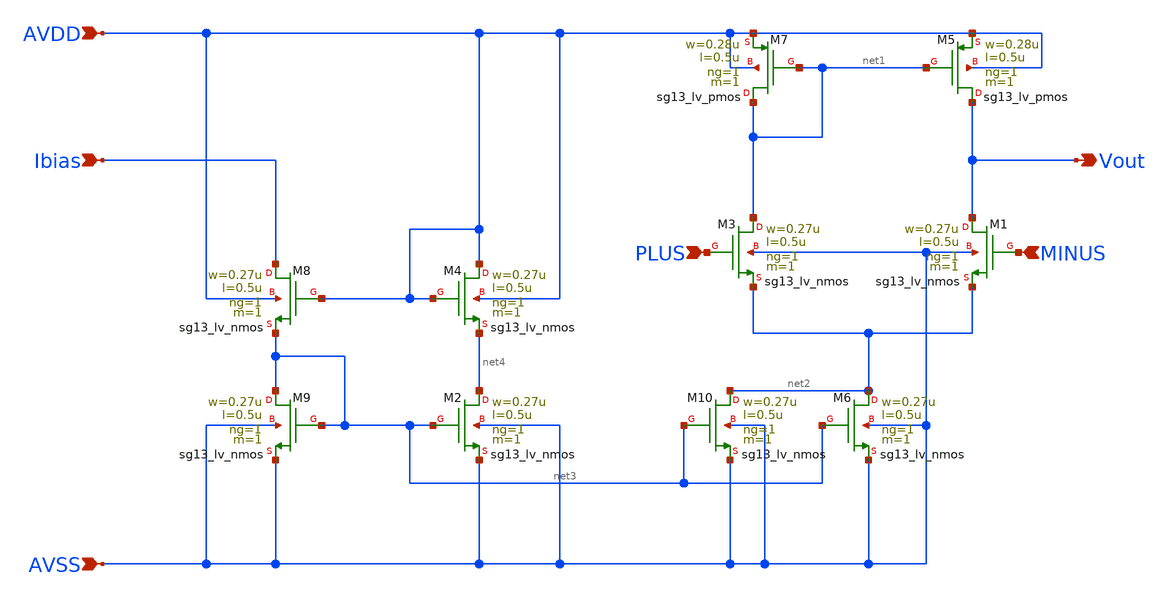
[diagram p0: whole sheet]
** sch_path: Designs/otas/5t_ota.sch
* (c) 2025 Thesis_HP, Apache-2.0 license
**.subckt 5t_ota PLUS MINUS Vout AVDD AVSS Ibias
*.ipin PLUS
*.ipin MINUS
*.opin Vout
*.ipin AVDD
*.ipin AVSS
*.ipin Ibias
XM1 Vout MINUS net2 AVSS sg13_lv_nmos w=0.27u l=0.5u ng=1 m=1 mm_ok=1
XM3 net1 PLUS net2 AVSS sg13_lv_nmos w=0.27u l=0.5u ng=1 m=1 mm_ok=1
XM5 Vout net1 AVDD AVDD sg13_lv_pmos w=0.28u l=0.5u ng=1 m=1 mm_ok=1
XM7 net1 net1 AVDD AVDD sg13_lv_pmos w=0.28u l=0.5u ng=1 m=1 mm_ok=1
XM6 net2 net3 AVSS AVSS sg13_lv_nmos w=0.27u l=0.5u ng=1 m=1 mm_ok=1
XM4 AVDD AVDD net4 AVDD sg13_lv_nmos w=0.27u l=0.5u ng=1 m=1 mm_ok=1
XM2 net4 net3 AVSS AVSS sg13_lv_nmos w=0.27u l=0.5u ng=1 m=1 mm_ok=1
XM9 net3 net3 AVSS AVSS sg13_lv_nmos w=0.27u l=0.5u ng=1 m=1 mm_ok=1
XM8 Ibias AVDD net3 AVDD sg13_lv_nmos w=0.27u l=0.5u ng=1 m=1 mm_ok=1
XM10 net2 net3 AVSS AVSS sg13_lv_nmos w=0.27u l=0.5u ng=1 m=1 mm_ok=1
**.ends
.end
